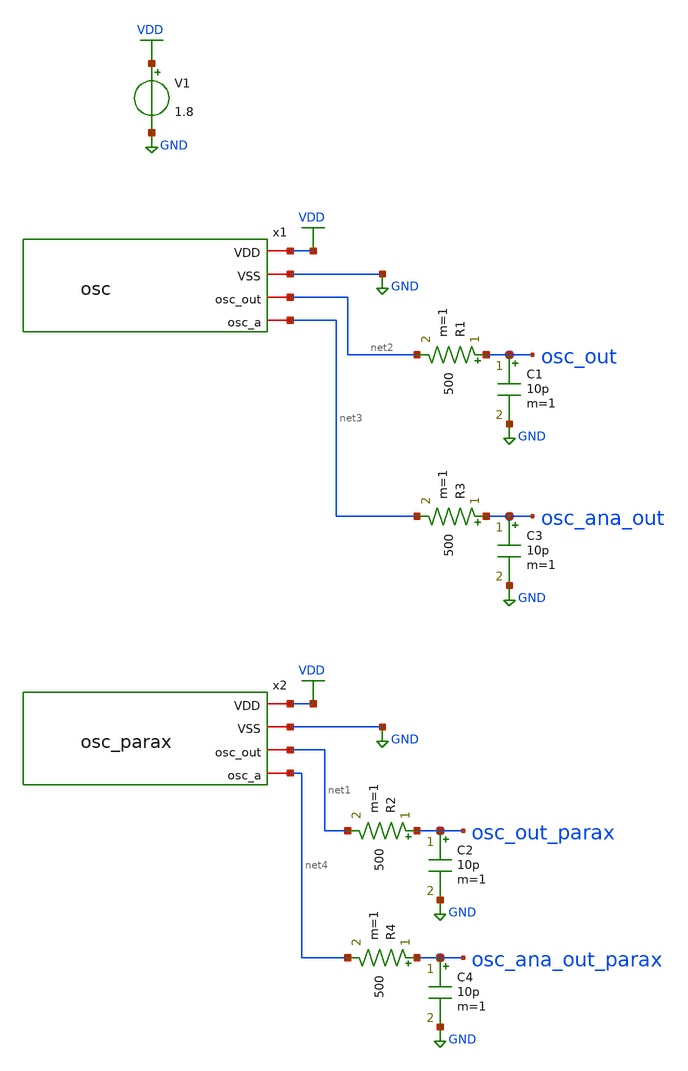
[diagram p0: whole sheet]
** sch_path: xschem/testbench.sch
**.subckt testbench
V1 VDD GND 1.8
x1 VDD GND net2 net3 osc
x2 VDD GND net1 net4 osc_parax
R1 osc_out net2 500 m=1
C1 osc_out GND 10p m=1
R2 osc_out_parax net1 500 m=1
C2 osc_out_parax GND 10p m=1
R3 osc_ana_out net3 500 m=1
C3 osc_ana_out GND 10p m=1
R4 osc_ana_out_parax net4 500 m=1
C4 osc_ana_out_parax GND 10p m=1
**** begin user architecture code

** opencircuitdesign pdks install
.lib $::SKYWATER_MODELS/sky130.lib.spice tt
.include $::SKYWATER_STDCELLS/sky130_fd_sc_hd.spice






.control
tran 500p 5u uic
write testbench.raw
*quit 0
.endc
.end


**** end user architecture code
**.ends

* expanding   symbol:  osc.sym # of pins=4
** sym_path: xschem/osc.sym
** sch_path: xschem/osc.sch
.subckt osc VDD VSS osc_out osc_a
*.iopin osc_out
*.iopin VDD
*.iopin VSS
*.iopin osc_a
XM1 osc_a osc_b left_cap VSS sky130_fd_pr__nfet_01v8 L=2 W=20 nf=1 ad='int((nf+1)/2) * W/nf * 0.29' as='int((nf+2)/2) * W/nf * 0.29'
+ pd='2*int((nf+1)/2) * (W/nf + 0.29)' ps='2*int((nf+2)/2) * (W/nf + 0.29)' nrd='0.29 / W' nrs='0.29 / W'
+ sa=0 sb=0 sd=0 mult=1 m=1
XM2 osc_b osc_a right_cap VSS sky130_fd_pr__nfet_01v8 L=2 W=20 nf=1 ad='int((nf+1)/2) * W/nf * 0.29'
+ as='int((nf+2)/2) * W/nf * 0.29' pd='2*int((nf+1)/2) * (W/nf + 0.29)' ps='2*int((nf+2)/2) * (W/nf + 0.29)'
+ nrd='0.29 / W' nrs='0.29 / W' sa=0 sb=0 sd=0 mult=1 m=1
XM3 osc_b osc_b VDD VDD sky130_fd_pr__pfet_01v8 L=2 W=20 nf=1 ad='int((nf+1)/2) * W/nf * 0.29' as='int((nf+2)/2) * W/nf * 0.29'
+ pd='2*int((nf+1)/2) * (W/nf + 0.29)' ps='2*int((nf+2)/2) * (W/nf + 0.29)' nrd='0.29 / W' nrs='0.29 / W'
+ sa=0 sb=0 sd=0 mult=1 m=1
XM4 osc_a osc_a VDD VDD sky130_fd_pr__pfet_01v8 L=2 W=20 nf=1 ad='int((nf+1)/2) * W/nf * 0.29' as='int((nf+2)/2) * W/nf * 0.29'
+ pd='2*int((nf+1)/2) * (W/nf + 0.29)' ps='2*int((nf+2)/2) * (W/nf + 0.29)' nrd='0.29 / W' nrs='0.29 / W'
+ sa=0 sb=0 sd=0 mult=1 m=1
XR1 osc_a VDD VSS sky130_fd_pr__res_high_po_0p35 L=18 mult=1 m=1
XR2 osc_b VDD VSS sky130_fd_pr__res_high_po_0p35 L=18 mult=1 m=1
XC1 right_cap left_cap sky130_fd_pr__cap_mim_m3_1 W=30 L=30 MF=5 m=5
XM5 cset cset VSS VSS sky130_fd_pr__nfet_01v8 L=2 W=20 nf=1 ad='int((nf+1)/2) * W/nf * 0.29' as='int((nf+2)/2) * W/nf * 0.29'
+ pd='2*int((nf+1)/2) * (W/nf + 0.29)' ps='2*int((nf+2)/2) * (W/nf + 0.29)' nrd='0.29 / W' nrs='0.29 / W'
+ sa=0 sb=0 sd=0 mult=1 m=1
XM6 left_cap cset VSS VSS sky130_fd_pr__nfet_01v8 L=2 W=20 nf=1 ad='int((nf+1)/2) * W/nf * 0.29' as='int((nf+2)/2) * W/nf * 0.29'
+ pd='2*int((nf+1)/2) * (W/nf + 0.29)' ps='2*int((nf+2)/2) * (W/nf + 0.29)' nrd='0.29 / W' nrs='0.29 / W'
+ sa=0 sb=0 sd=0 mult=1 m=1
XR3 cset VDD VSS sky130_fd_pr__res_high_po_0p35 L=20 mult=1 m=1
XM8 right_cap cset VSS VSS sky130_fd_pr__nfet_01v8 L=2 W=20 nf=1 ad='int((nf+1)/2) * W/nf * 0.29' as='int((nf+2)/2) * W/nf * 0.29'
+ pd='2*int((nf+1)/2) * (W/nf + 0.29)' ps='2*int((nf+2)/2) * (W/nf + 0.29)' nrd='0.29 / W' nrs='0.29 / W'
+ sa=0 sb=0 sd=0 mult=1 m=1
x1 osc_a VSS VSS VDD VDD osc_out sky130_fd_sc_hd__clkinv_8
XC2 left_cap right_cap sky130_fd_pr__cap_mim_m3_1 W=30 L=30 MF=5 m=5
.ends


* expanding   symbol:  osc_parax.sym # of pins=4
** sym_path: xschem/osc.sym
.include ../../mag/osc.sim.spice
.GLOBAL GND
.GLOBAL VDD
.end
